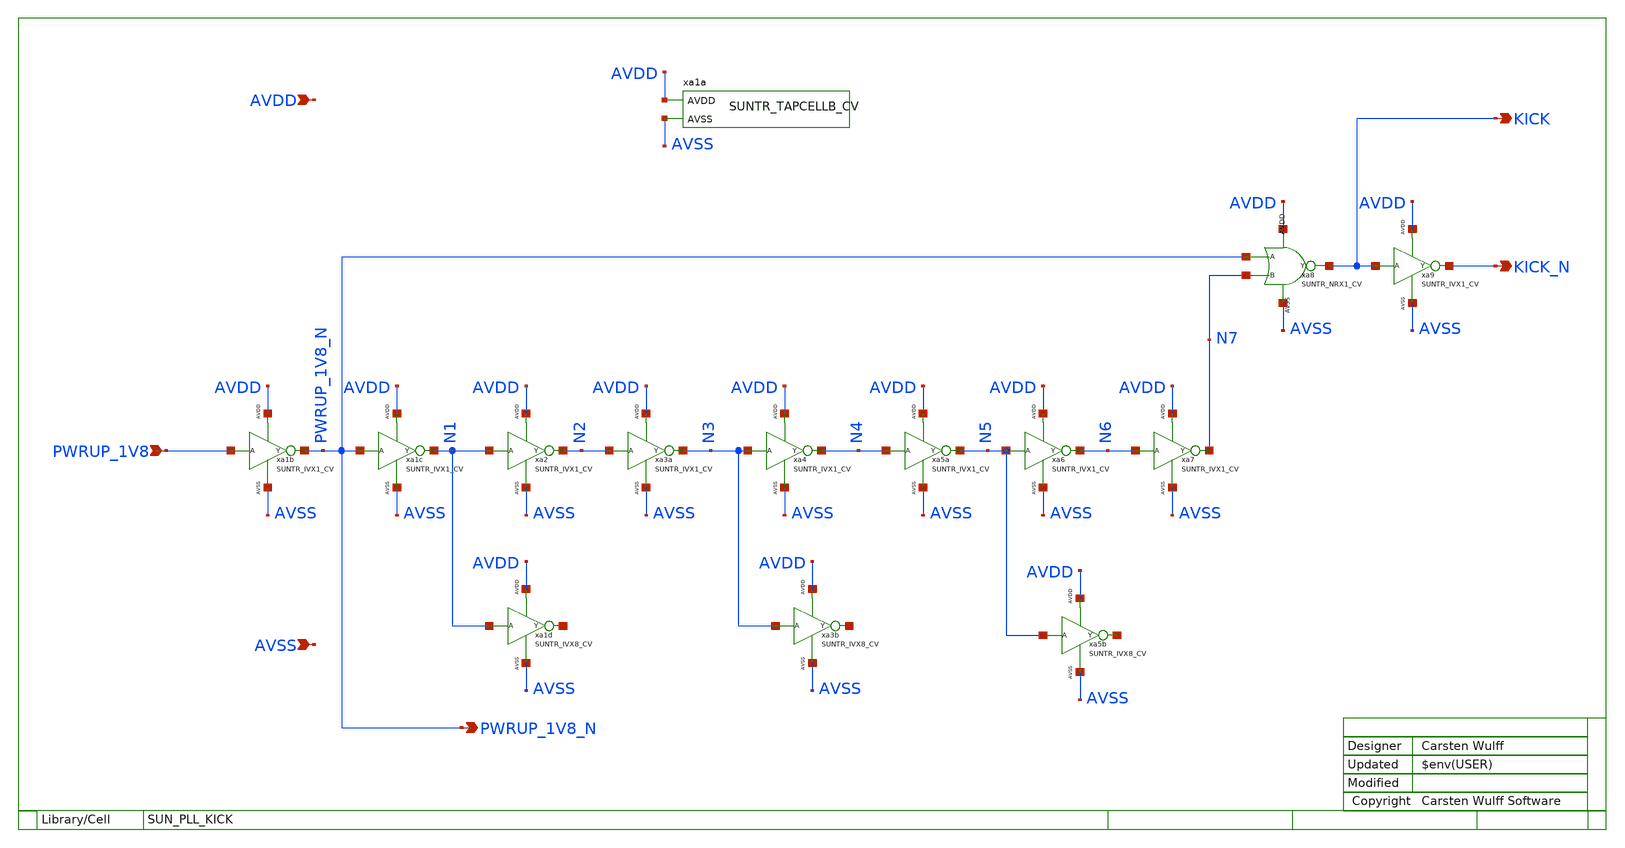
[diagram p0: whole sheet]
** sch_path: ip/sun_pll_sky130nm/design/SUN_PLL_SKY130NM/SUN_PLL_KICK.sch
**.subckt SUN_PLL_KICK PWRUP_1V8 KICK KICK_N AVDD AVSS PWRUP_1V8_N
*.ipin PWRUP_1V8
*.opin KICK
*.opin KICK_N
*.ipin AVDD
*.ipin AVSS
*.opin PWRUP_1V8_N
xa1c PWRUP_1V8_N N1 AVDD AVSS SUNTR_IVX1_CV
xa2 N1 N2 AVDD AVSS SUNTR_IVX1_CV
xa3a N2 N3 AVDD AVSS SUNTR_IVX1_CV
xa4 N3 N4 AVDD AVSS SUNTR_IVX1_CV
xa5a N4 N5 AVDD AVSS SUNTR_IVX1_CV
xa6 N5 N6 AVDD AVSS SUNTR_IVX1_CV
xa7 N6 N7 AVDD AVSS SUNTR_IVX1_CV
xa8 PWRUP_1V8_N N7 KICK AVDD AVSS SUNTR_NRX1_CV
xa9 KICK KICK_N AVDD AVSS SUNTR_IVX1_CV
xa1a AVDD AVSS SUNTR_TAPCELLB_CV
xa1b PWRUP_1V8 PWRUP_1V8_N AVDD AVSS SUNTR_IVX1_CV
xa1d AVSS AVDD N1 net1 SUNTR_IVX8_CV
xa3b AVSS AVDD N3 net2 SUNTR_IVX8_CV
xa5b AVSS AVDD N5 net3 SUNTR_IVX8_CV
**.ends
.end
